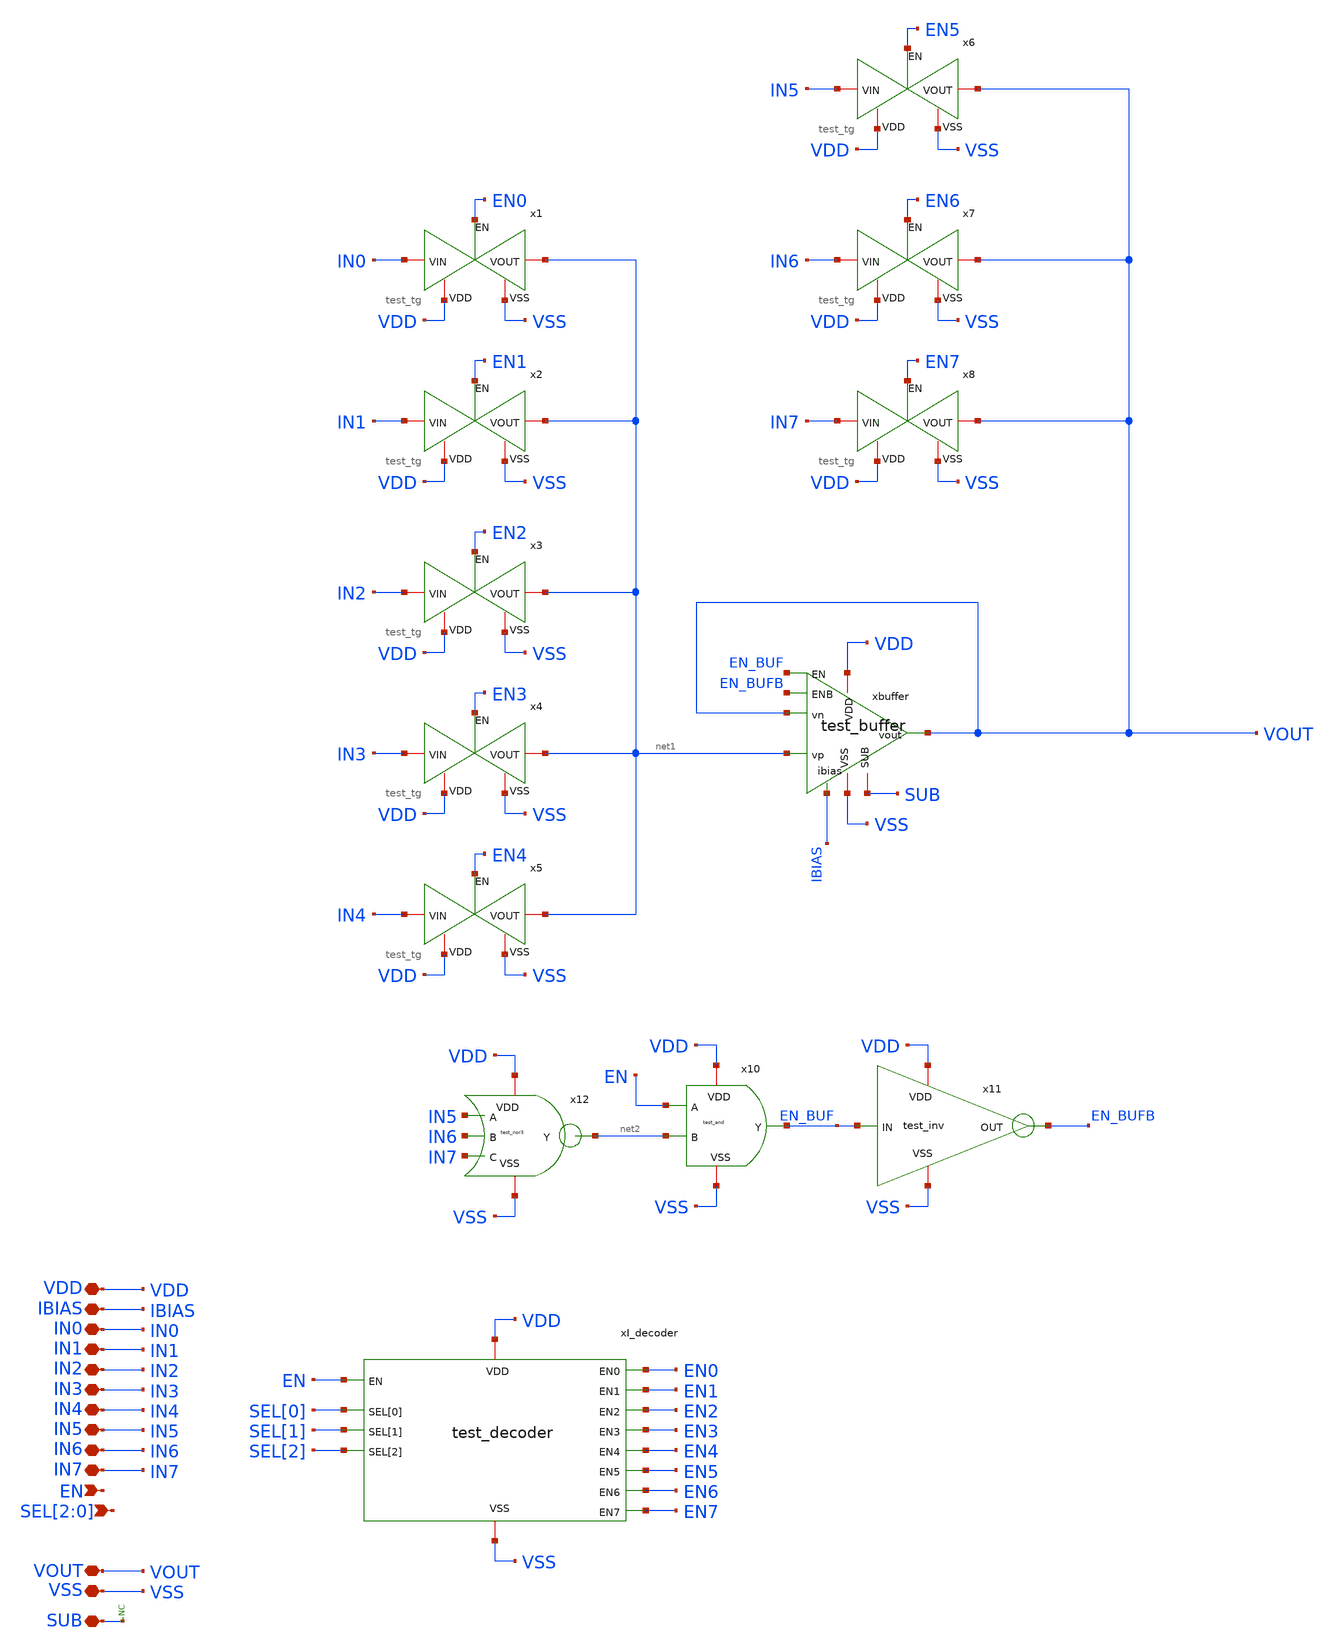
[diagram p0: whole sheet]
** sch_path: designs/libs/core_test/test/test.sch
**.subckt test VDD VSS SUB VOUT IBIAS EN SEL[2],SEL[1],SEL[0] IN0 IN1 IN2 IN3 IN4 IN5 IN6 IN7
*.iopin VDD
*.iopin VSS
*.iopin SUB
*.iopin VOUT
*.iopin IBIAS
*.ipin EN
*.ipin SEL[2],SEL[1],SEL[0]
*.iopin IN0
*.iopin IN1
*.iopin IN2
*.iopin IN3
*.iopin IN4
*.iopin IN5
*.iopin IN6
*.iopin IN7
* noconn SUB
x1 VDD EN0 IN0 net1 VSS test_tg
x2 VDD EN1 IN1 net1 VSS test_tg
x3 VDD EN2 IN2 net1 VSS test_tg
x4 VDD EN3 IN3 net1 VSS test_tg
x5 VDD EN4 IN4 net1 VSS test_tg
x6 VDD EN5 IN5 VOUT VSS test_tg
x7 VDD EN6 IN6 VOUT VSS test_tg
x8 VDD EN7 IN7 VOUT VSS test_tg
xbuffer VDD IBIAS VOUT net1 VOUT VSS EN_BUF EN_BUFB SUB test_buffer
xI_decoder SEL[0] SEL[1] SEL[2] VDD VSS EN0 EN1 EN2 EN3 EN4 EN5 EN6 EN7 EN test_decoder
x10 VDD EN EN_BUF net2 VSS test_and
x11 VDD EN_BUFB EN_BUF VSS test_inv
x12 IN5 IN6 IN7 VDD net2 VSS test_nor3
**.ends
.end
